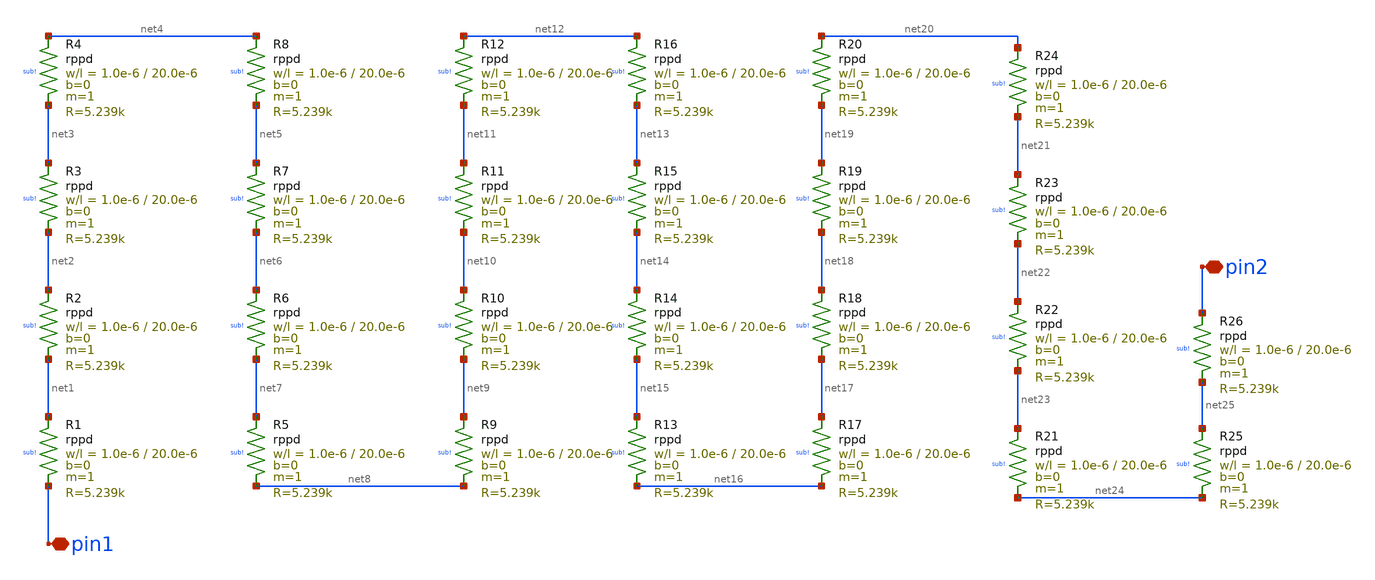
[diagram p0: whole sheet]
** sch_path: ihp-sg13g2/libs.ref/sg13g2_io/xschem/sg13g2_RCClampResistor.sch
**.subckt sg13g2_RCClampResistor pin1 pin2
*.iopin pin1
*.iopin pin2
XR1 net1 pin1 sub! rppd w=1.0e-6 l=20.0e-6 m=1 b=0 mm_ok=1
XR2 net2 net1 sub! rppd w=1.0e-6 l=20.0e-6 m=1 b=0 mm_ok=1
XR3 net3 net2 sub! rppd w=1.0e-6 l=20.0e-6 m=1 b=0 mm_ok=1
XR4 net4 net3 sub! rppd w=1.0e-6 l=20.0e-6 m=1 b=0 mm_ok=1
XR5 net7 net8 sub! rppd w=1.0e-6 l=20.0e-6 m=1 b=0 mm_ok=1
XR6 net6 net7 sub! rppd w=1.0e-6 l=20.0e-6 m=1 b=0 mm_ok=1
XR7 net5 net6 sub! rppd w=1.0e-6 l=20.0e-6 m=1 b=0 mm_ok=1
XR8 net4 net5 sub! rppd w=1.0e-6 l=20.0e-6 m=1 b=0 mm_ok=1
XR9 net9 net8 sub! rppd w=1.0e-6 l=20.0e-6 m=1 b=0 mm_ok=1
XR10 net10 net9 sub! rppd w=1.0e-6 l=20.0e-6 m=1 b=0 mm_ok=1
XR11 net11 net10 sub! rppd w=1.0e-6 l=20.0e-6 m=1 b=0 mm_ok=1
XR12 net12 net11 sub! rppd w=1.0e-6 l=20.0e-6 m=1 b=0 mm_ok=1
XR13 net15 net16 sub! rppd w=1.0e-6 l=20.0e-6 m=1 b=0 mm_ok=1
XR14 net14 net15 sub! rppd w=1.0e-6 l=20.0e-6 m=1 b=0 mm_ok=1
XR15 net13 net14 sub! rppd w=1.0e-6 l=20.0e-6 m=1 b=0 mm_ok=1
XR16 net12 net13 sub! rppd w=1.0e-6 l=20.0e-6 m=1 b=0 mm_ok=1
XR17 net17 net16 sub! rppd w=1.0e-6 l=20.0e-6 m=1 b=0 mm_ok=1
XR18 net18 net17 sub! rppd w=1.0e-6 l=20.0e-6 m=1 b=0 mm_ok=1
XR19 net19 net18 sub! rppd w=1.0e-6 l=20.0e-6 m=1 b=0 mm_ok=1
XR20 net20 net19 sub! rppd w=1.0e-6 l=20.0e-6 m=1 b=0 mm_ok=1
XR21 net23 net24 sub! rppd w=1.0e-6 l=20.0e-6 m=1 b=0 mm_ok=1
XR22 net22 net23 sub! rppd w=1.0e-6 l=20.0e-6 m=1 b=0 mm_ok=1
XR23 net21 net22 sub! rppd w=1.0e-6 l=20.0e-6 m=1 b=0 mm_ok=1
XR24 net20 net21 sub! rppd w=1.0e-6 l=20.0e-6 m=1 b=0 mm_ok=1
XR25 net25 net24 sub! rppd w=1.0e-6 l=20.0e-6 m=1 b=0 mm_ok=1
XR26 pin2 net25 sub! rppd w=1.0e-6 l=20.0e-6 m=1 b=0 mm_ok=1
**.ends
.end
